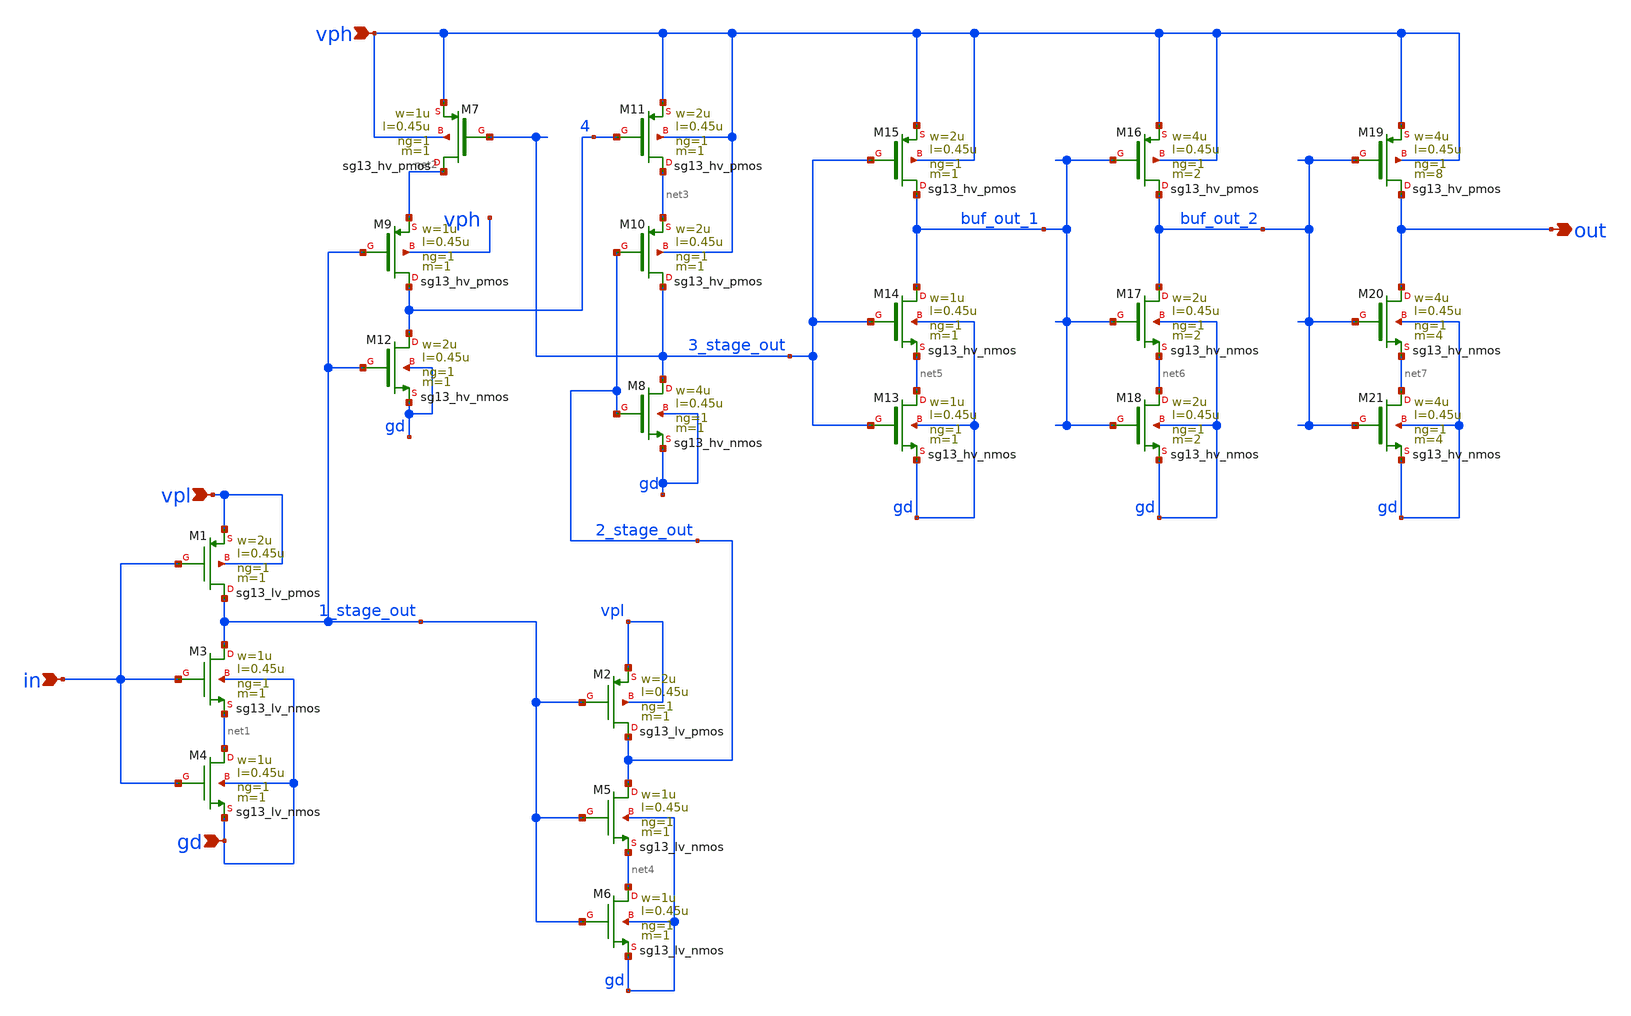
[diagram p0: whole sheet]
** sch_path: schematics/misc/level_shifter.sch
**.subckt level_shifter in out gd vph vpl
*.ipin in
*.opin out
*.ipin gd
*.ipin vph
*.ipin vpl
XM1 1_stage_out in vpl vpl sg13_lv_pmos w=2u l=0.45u ng=1 m=1 mm_ok=1
XM3 1_stage_out in net1 gd sg13_lv_nmos w=1u l=0.45u ng=1 m=1 mm_ok=1
XM4 net1 in gd gd sg13_lv_nmos w=1u l=0.45u ng=1 m=1 mm_ok=1
XM2 2_stage_out 1_stage_out vpl vpl sg13_lv_pmos w=2u l=0.45u ng=1 m=1 mm_ok=1
XM5 2_stage_out 1_stage_out net4 gd sg13_lv_nmos w=1u l=0.45u ng=1 m=1 mm_ok=1
XM6 net4 1_stage_out gd gd sg13_lv_nmos w=1u l=0.45u ng=1 m=1 mm_ok=1
XM7 net2 3_stage_out vph vph sg13_hv_pmos w=1u l=0.45u ng=1 m=1 mm_ok=1
XM8 3_stage_out 2_stage_out gd gd sg13_hv_nmos w=4u l=0.45u ng=1 m=1 mm_ok=1
XM9 4 1_stage_out net2 vph sg13_hv_pmos w=1u l=0.45u ng=1 m=1 mm_ok=1
XM10 3_stage_out 2_stage_out net3 vph sg13_hv_pmos w=2u l=0.45u ng=1 m=1 mm_ok=1
XM11 net3 4 vph vph sg13_hv_pmos w=2u l=0.45u ng=1 m=1 mm_ok=1
XM12 4 1_stage_out gd gd sg13_hv_nmos w=2u l=0.45u ng=1 m=1 mm_ok=1
XM15 buf_out_1 3_stage_out vph vph sg13_hv_pmos w=2u l=0.45u ng=1 m=1 mm_ok=1
XM14 buf_out_1 3_stage_out net5 gd sg13_hv_nmos w=1u l=0.45u ng=1 m=1 mm_ok=1
XM13 net5 3_stage_out gd gd sg13_hv_nmos w=1u l=0.45u ng=1 m=1 mm_ok=1
XM16 buf_out_2 buf_out_1 vph vph sg13_hv_pmos w=4u l=0.45u ng=1 m=2 mm_ok=1
XM17 buf_out_2 buf_out_1 net6 gd sg13_hv_nmos w=2u l=0.45u ng=1 m=2 mm_ok=1
XM18 net6 buf_out_1 gd gd sg13_hv_nmos w=2u l=0.45u ng=1 m=2 mm_ok=1
XM19 out buf_out_2 vph vph sg13_hv_pmos w=4u l=0.45u ng=1 m=8 mm_ok=1
XM20 out buf_out_2 net7 gd sg13_hv_nmos w=4u l=0.45u ng=1 m=4 mm_ok=1
XM21 net7 buf_out_2 gd gd sg13_hv_nmos w=4u l=0.45u ng=1 m=4 mm_ok=1
**.ends
.end
